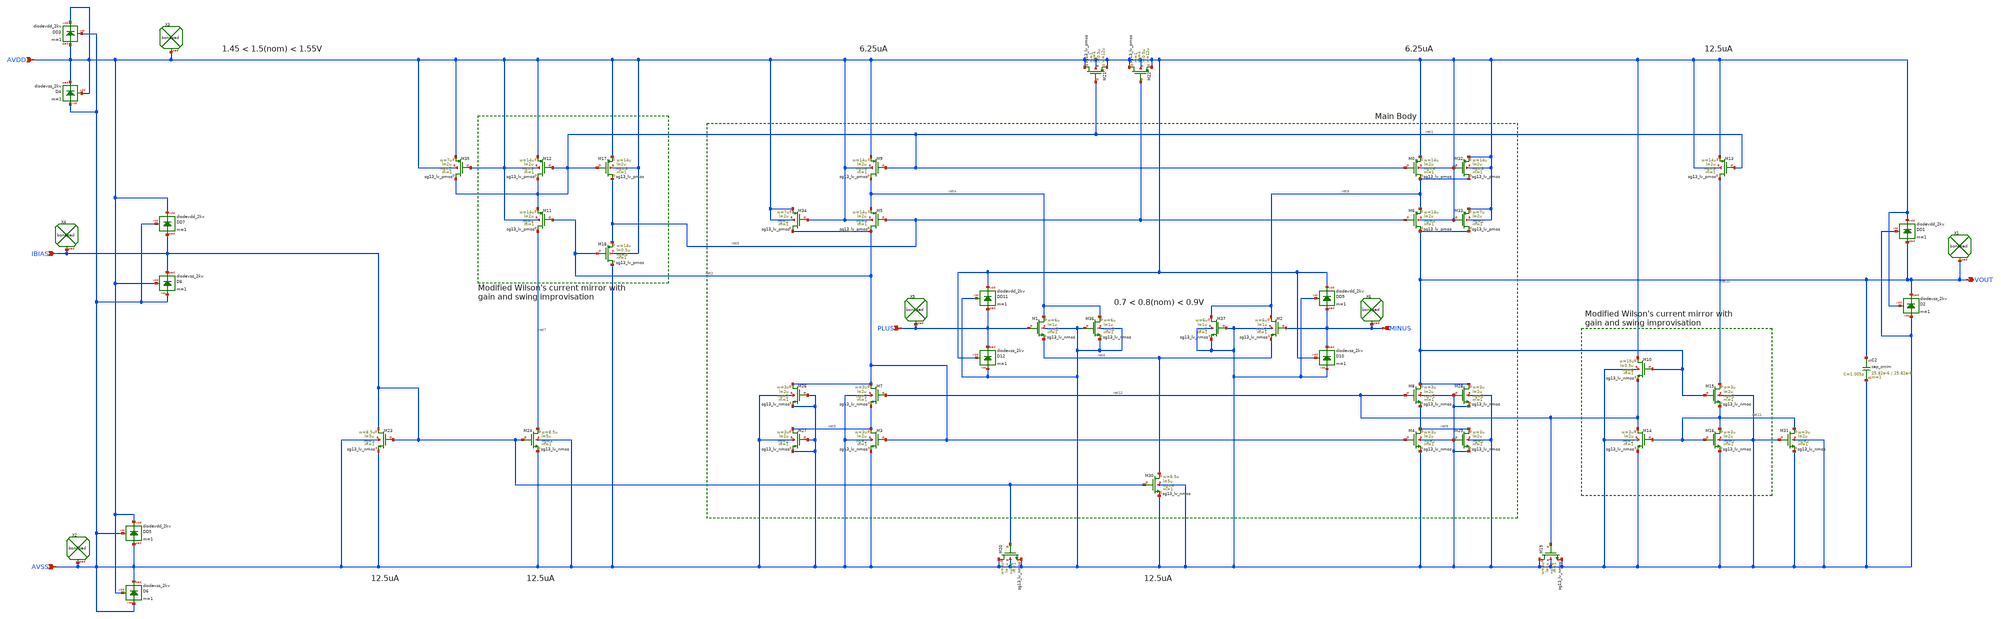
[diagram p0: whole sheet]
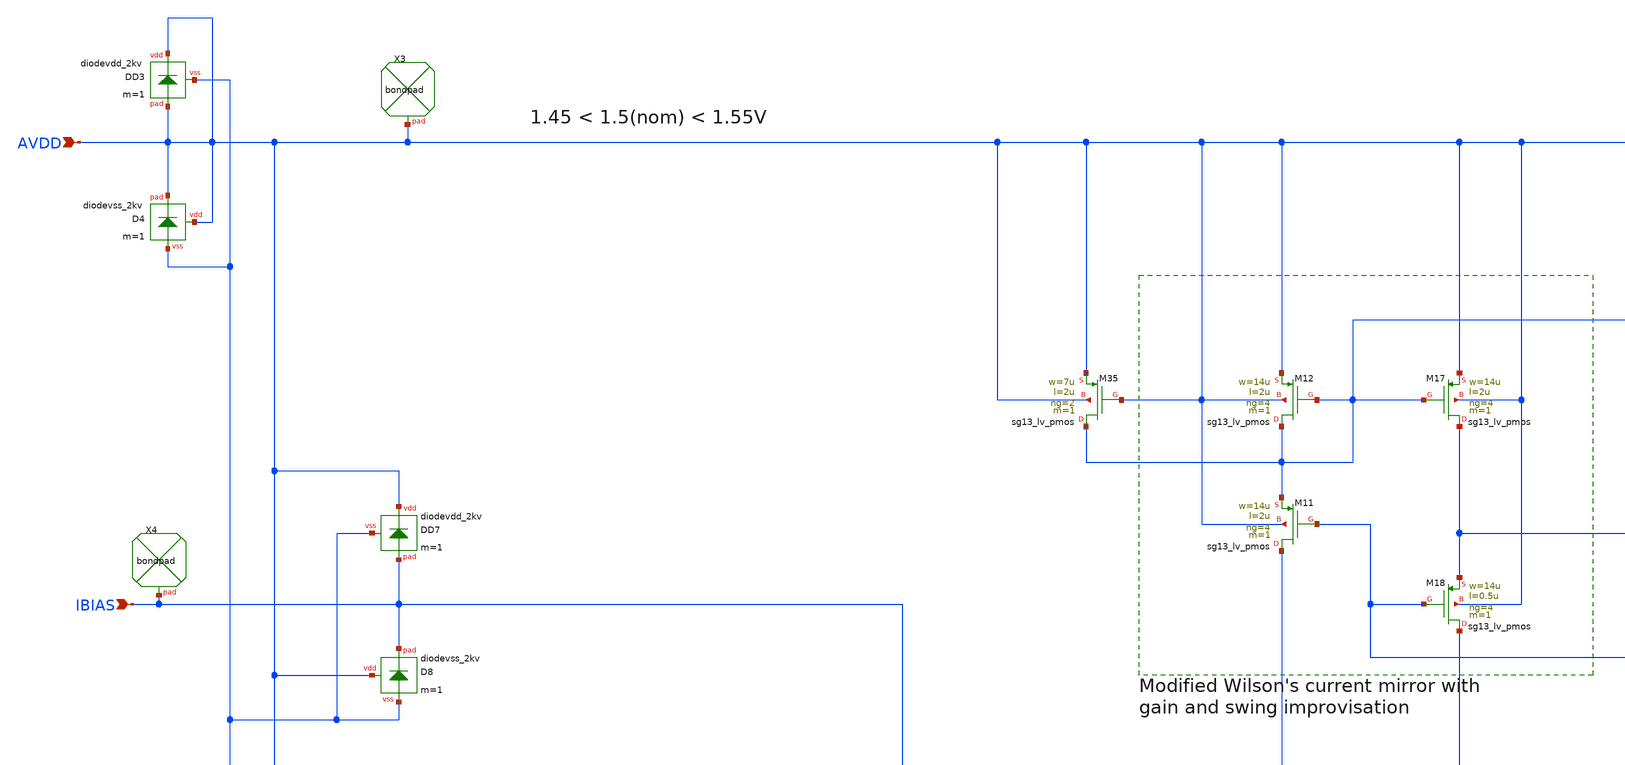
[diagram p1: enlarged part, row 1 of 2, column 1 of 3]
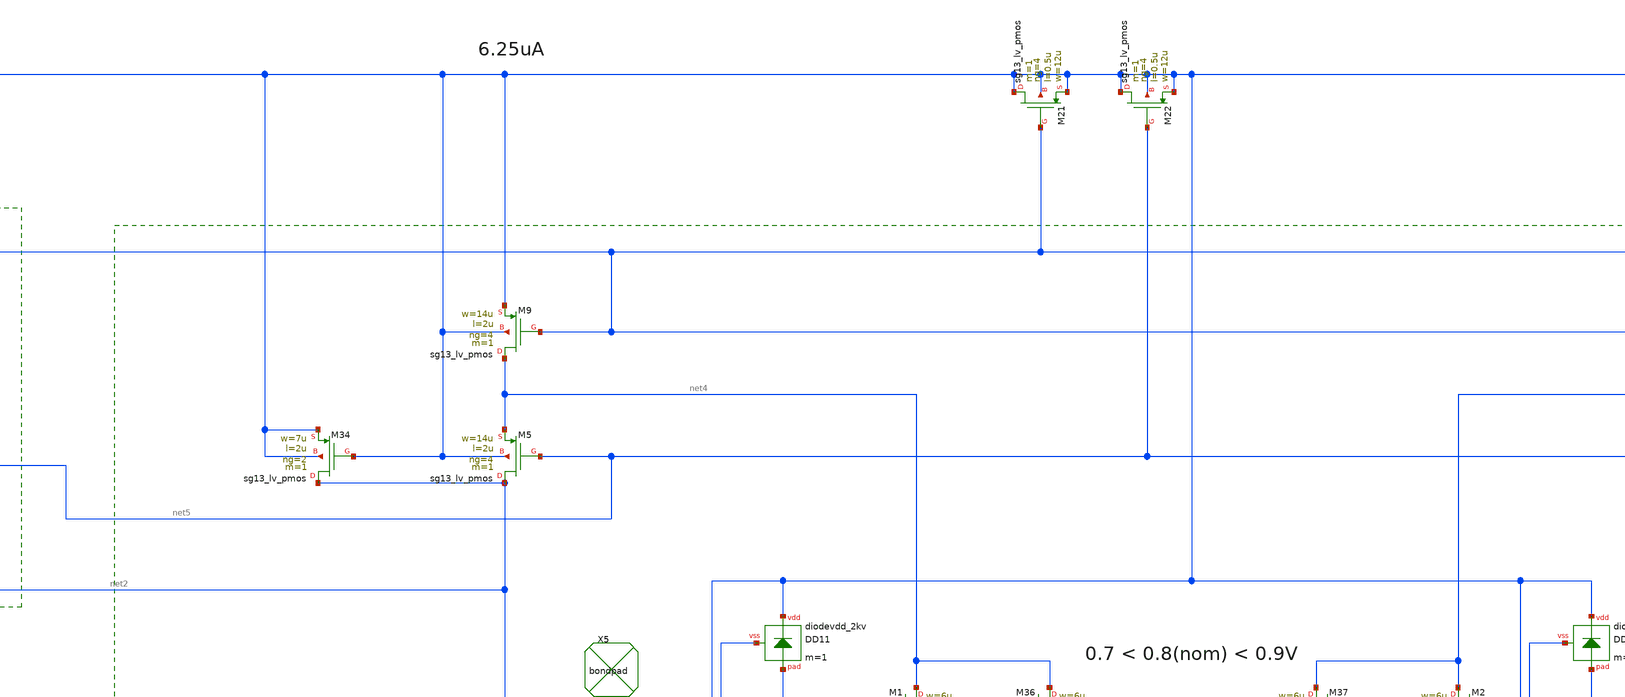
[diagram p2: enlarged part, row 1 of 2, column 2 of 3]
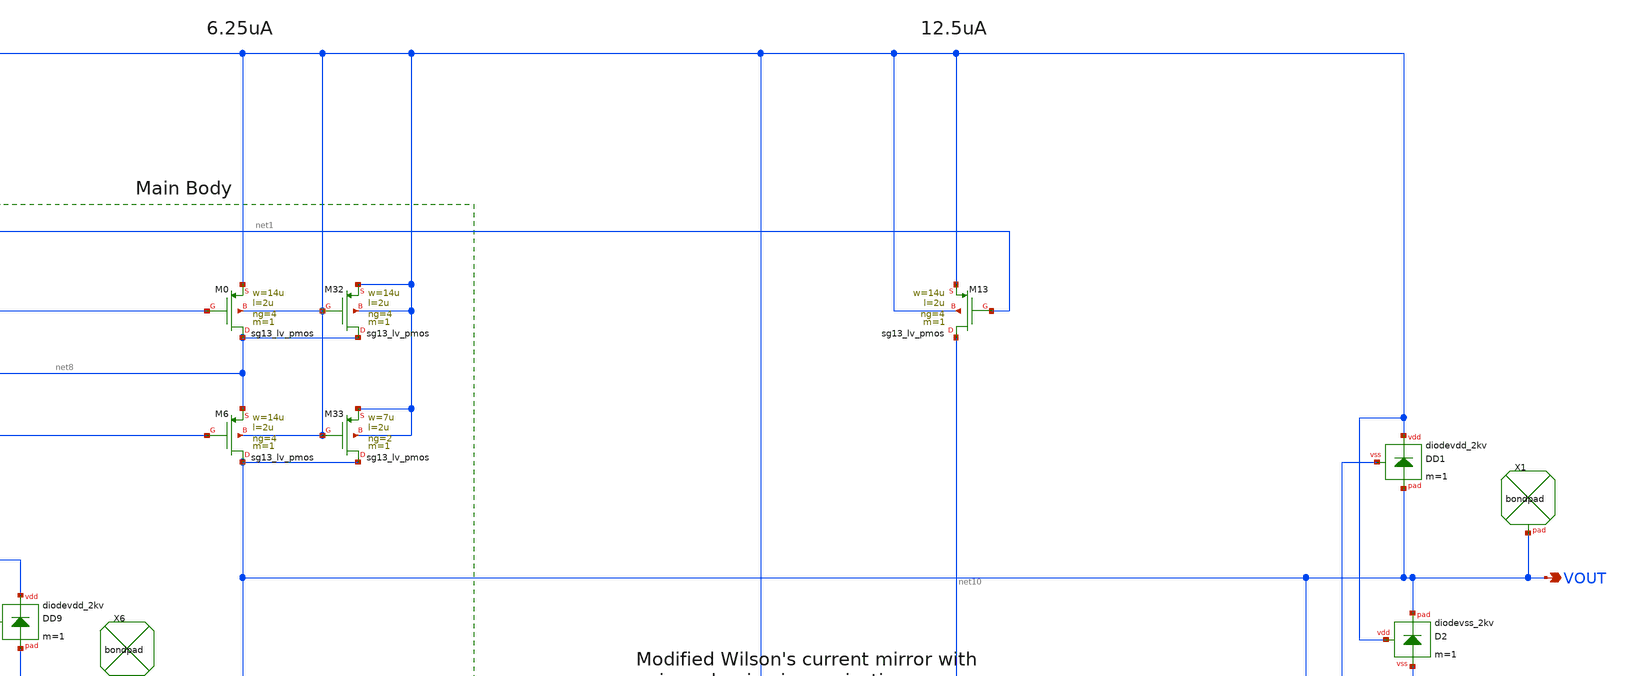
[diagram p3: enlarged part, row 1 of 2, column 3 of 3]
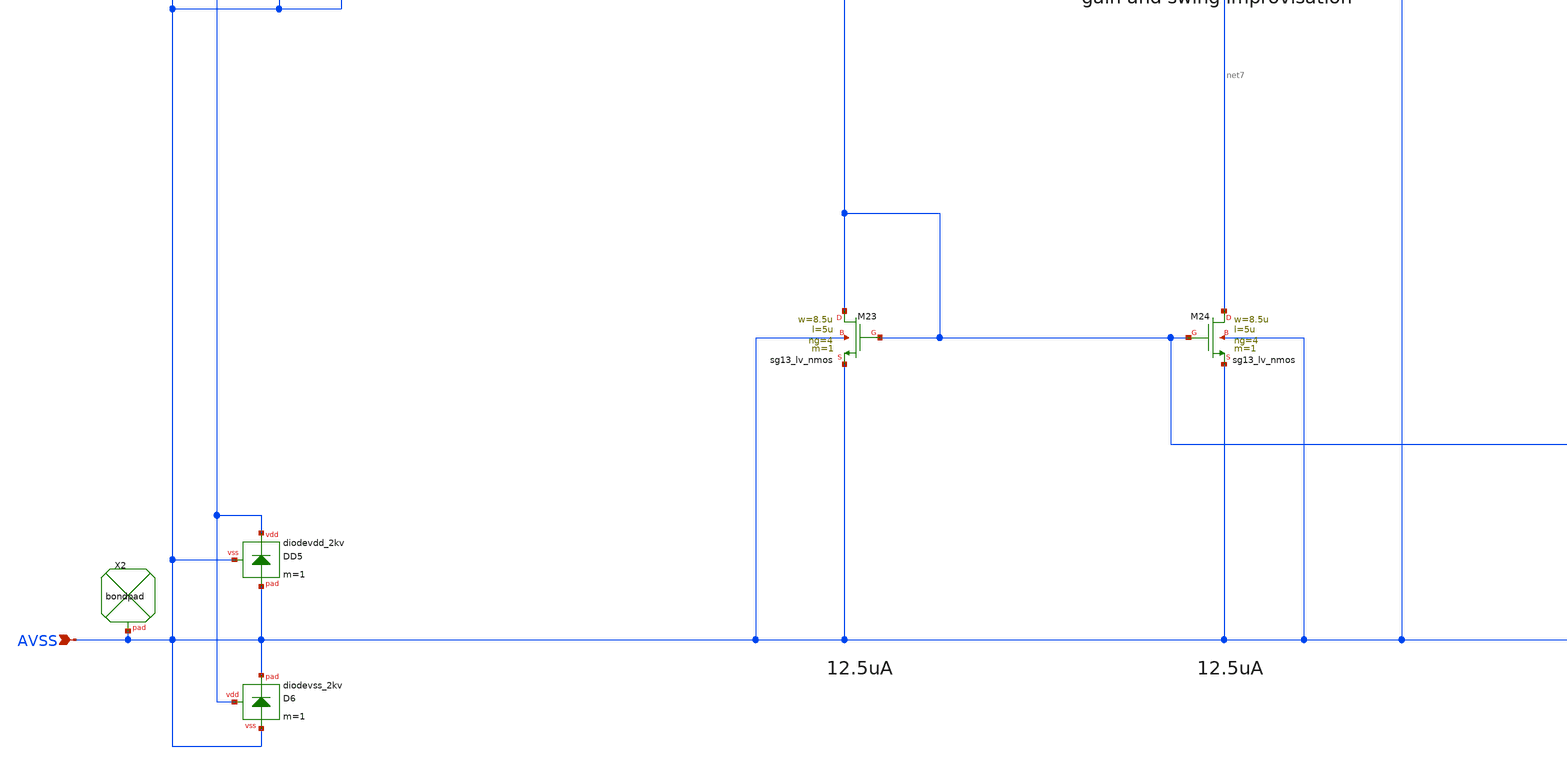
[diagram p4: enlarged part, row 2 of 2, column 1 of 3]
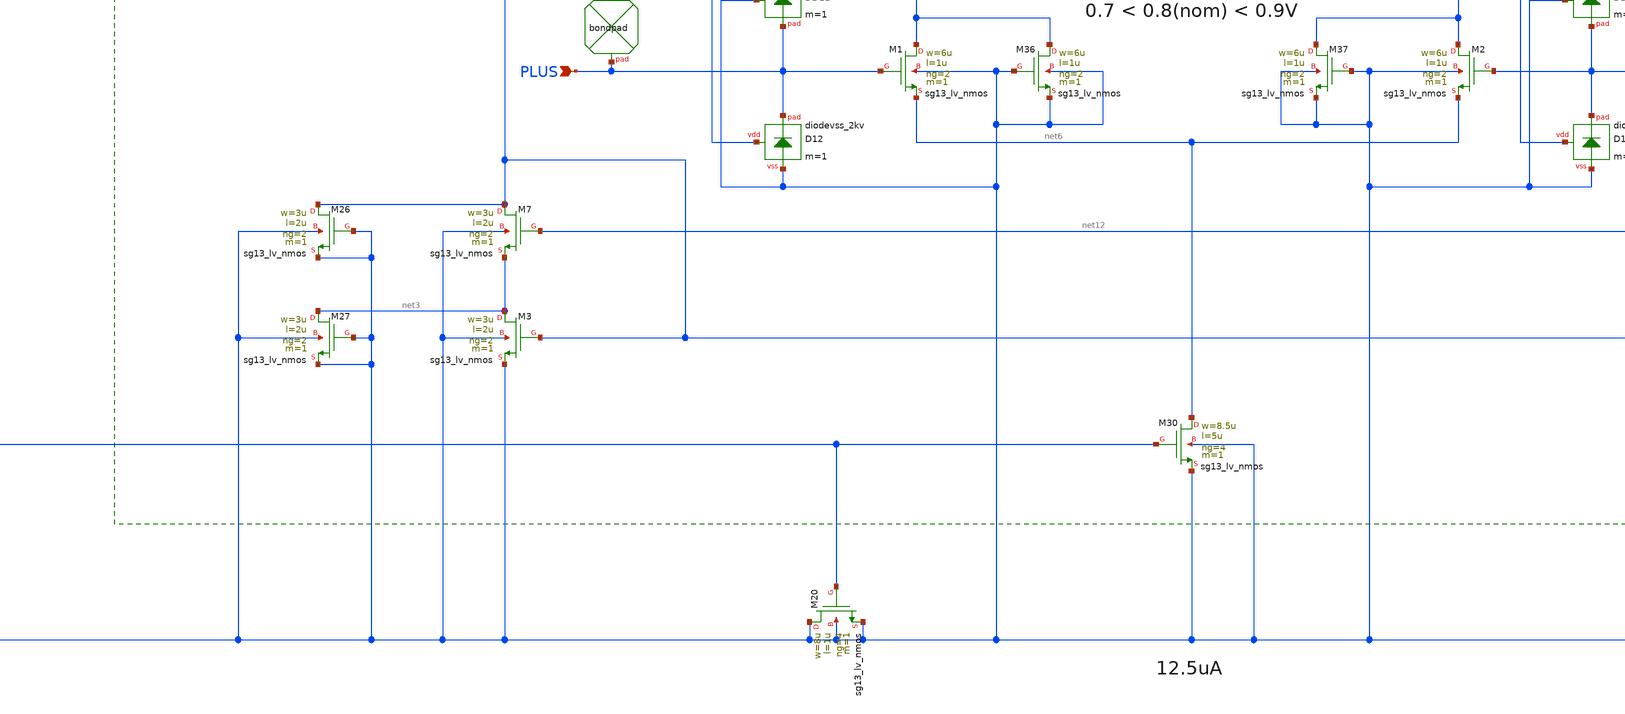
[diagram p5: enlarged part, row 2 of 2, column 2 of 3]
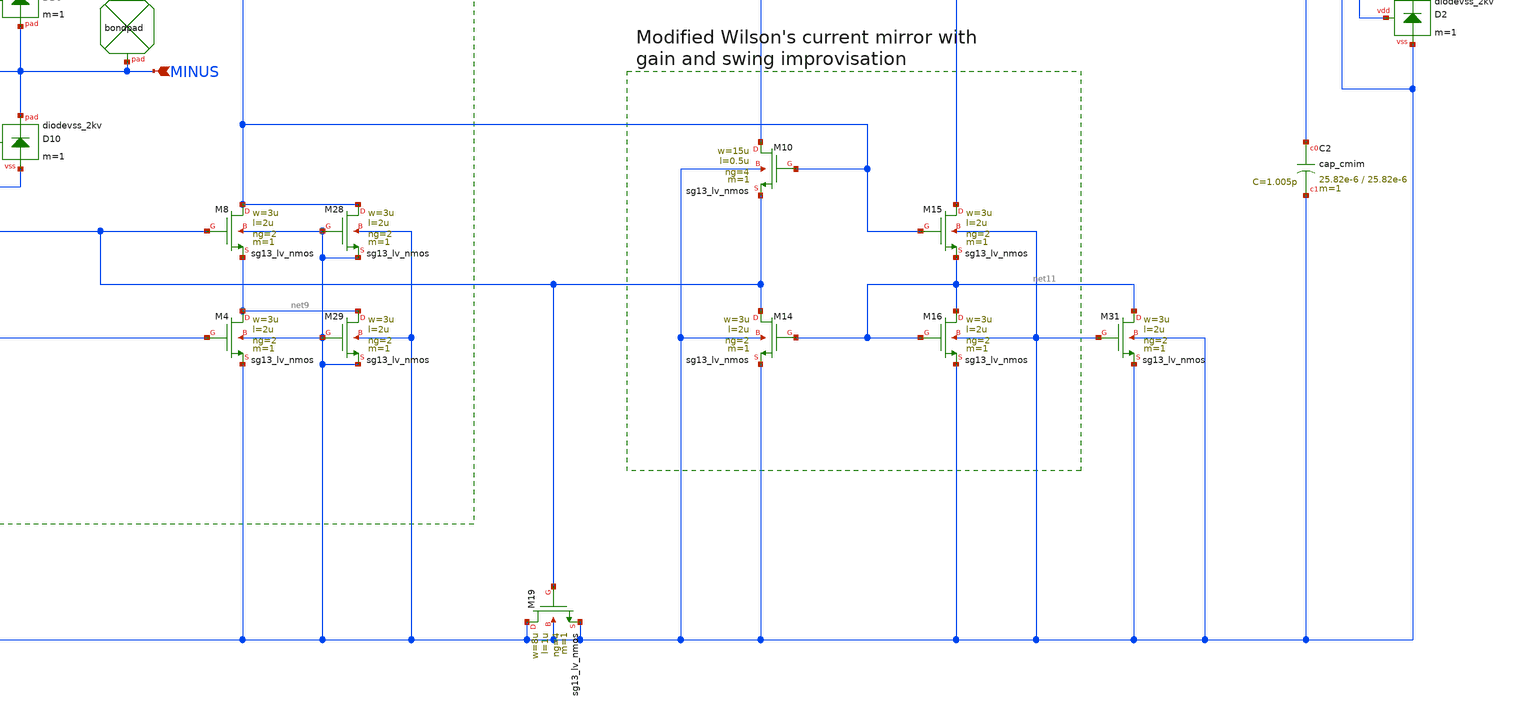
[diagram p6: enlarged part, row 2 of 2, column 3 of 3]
** sch_path: Amplifier_with_decoupling/design_data/xschem/FMD_QNC_ota_decoup.sch
* (c) 2025 Thesis_HP, Apache-2.0 license
**.subckt FMD_QNC_ota_decoup PLUS MINUS VOUT AVSS IBIAS AVDD
*.ipin PLUS
*.ipin MINUS
*.opin VOUT
*.ipin AVSS
*.ipin IBIAS
*.ipin AVDD
XM23 IBIAS IBIAS AVSS AVSS sg13_lv_nmos w=8.5u l=5u ng=4 m=1 mm_ok=1
XM24 net7 IBIAS AVSS AVSS sg13_lv_nmos w=8.5u l=5u ng=4 m=1 mm_ok=1
XM11 net7 net2 net1 AVDD sg13_lv_pmos w=14u l=2u ng=4 m=1 mm_ok=1
XM12 net1 net1 AVDD AVDD sg13_lv_pmos w=14u l=2u ng=4 m=1 mm_ok=1
XM18 AVSS net2 net5 AVDD sg13_lv_pmos w=14u l=0.5u ng=4 m=1 mm_ok=1
XM17 net5 net1 AVDD AVDD sg13_lv_pmos w=14u l=2u ng=4 m=1 mm_ok=1
XM9 net4 net1 AVDD AVDD sg13_lv_pmos w=14u l=2u ng=4 m=1 mm_ok=1
XM5 net2 net5 net4 AVDD sg13_lv_pmos w=14u l=2u ng=4 m=1 mm_ok=1
XM7 net2 net12 net3 AVSS sg13_lv_nmos w=3u l=2u ng=2 m=1 mm_ok=1
XM3 net3 net2 AVSS AVSS sg13_lv_nmos w=3u l=2u ng=2 m=1 mm_ok=1
XM30 net6 IBIAS AVSS AVSS sg13_lv_nmos w=8.5u l=5u ng=4 m=1 mm_ok=1
XM1 net4 PLUS net6 AVSS sg13_lv_nmos w=6u l=1u ng=2 m=1 mm_ok=1
XM2 net8 MINUS net6 AVSS sg13_lv_nmos w=6u l=1u ng=2 m=1 mm_ok=1
XM37 net8 AVSS AVSS AVSS sg13_lv_nmos w=6u l=1u ng=2 m=1 mm_ok=1
XM6 VOUT net5 net8 AVDD sg13_lv_pmos w=14u l=2u ng=4 m=1 mm_ok=1
XM0 net8 net1 AVDD AVDD sg13_lv_pmos w=14u l=2u ng=4 m=1 mm_ok=1
XM8 VOUT net12 net9 AVSS sg13_lv_nmos w=3u l=2u ng=2 m=1 mm_ok=1
XM4 net9 net2 AVSS AVSS sg13_lv_nmos w=3u l=2u ng=2 m=1 mm_ok=1
XM29 net9 AVSS AVSS AVSS sg13_lv_nmos w=3u l=2u ng=2 m=1 mm_ok=1
XM28 VOUT AVSS AVSS AVSS sg13_lv_nmos w=3u l=2u ng=2 m=1 mm_ok=1
XM32 net8 AVDD AVDD AVDD sg13_lv_pmos w=14u l=2u ng=4 m=1 mm_ok=1
XM33 VOUT AVDD AVDD AVDD sg13_lv_pmos w=7u l=2u ng=2 m=1 mm_ok=1
XM13 net10 net1 AVDD AVDD sg13_lv_pmos w=14u l=2u ng=4 m=1 mm_ok=1
XM15 net10 VOUT net11 AVSS sg13_lv_nmos w=3u l=2u ng=2 m=1 mm_ok=1
XM16 net11 net11 AVSS AVSS sg13_lv_nmos w=3u l=2u ng=2 m=1 mm_ok=1
XM14 net12 net11 AVSS AVSS sg13_lv_nmos w=3u l=2u ng=2 m=1 mm_ok=1
XM10 AVDD VOUT net12 AVSS sg13_lv_nmos w=15u l=0.5u ng=4 m=1 mm_ok=1
XM36 net4 AVSS AVSS AVSS sg13_lv_nmos w=6u l=1u ng=2 m=1 mm_ok=1
XM34 net2 AVDD AVDD AVDD sg13_lv_pmos w=7u l=2u ng=2 m=1 mm_ok=1
XM27 net3 AVSS AVSS AVSS sg13_lv_nmos w=3u l=2u ng=2 m=1 mm_ok=1
XM26 net2 AVSS AVSS AVSS sg13_lv_nmos w=3u l=2u ng=2 m=1 mm_ok=1
XM35 net1 AVDD AVDD AVDD sg13_lv_pmos w=7u l=2u ng=2 m=1 mm_ok=1
XM31 net11 AVSS AVSS AVSS sg13_lv_nmos w=3u l=2u ng=2 m=1 mm_ok=1
XC2 VOUT AVSS cap_cmim w=25.82e-6 l=25.82e-6 m=1 mm_ok=1
XM19 AVSS net12 AVSS AVSS sg13_lv_nmos w=8u l=1u ng=4 m=1 mm_ok=1
XM20 AVSS IBIAS AVSS AVSS sg13_lv_nmos w=8u l=1u ng=4 m=1 mm_ok=1
XM21 AVDD net1 AVDD AVDD sg13_lv_pmos w=12u l=0.5u ng=4 m=1 mm_ok=1
XM22 AVDD net5 AVDD AVDD sg13_lv_pmos w=12u l=0.5u ng=4 m=1 mm_ok=1
XX1 VOUT bondpad size=80u shape=0 padtype=0
XD1 AVDD VOUT AVSS diodevdd_2kv m=1
XD2 AVDD VOUT AVSS diodevss_2kv m=1
XX5 PLUS bondpad size=80u shape=0 padtype=0
XD9 AVDD MINUS AVSS diodevdd_2kv m=1
XD10 AVDD MINUS AVSS diodevss_2kv m=1
XX6 MINUS bondpad size=80u shape=0 padtype=0
XD11 AVDD PLUS AVSS diodevdd_2kv m=1
XD12 AVDD PLUS AVSS diodevss_2kv m=1
XD3 AVDD AVDD AVSS diodevdd_2kv m=1
XD4 AVDD AVDD AVSS diodevss_2kv m=1
XD5 AVDD AVSS AVSS diodevdd_2kv m=1
XD6 AVDD AVSS AVSS diodevss_2kv m=1
XX2 AVSS bondpad size=80u shape=0 padtype=0
XX3 AVDD bondpad size=80u shape=0 padtype=0
XD7 AVDD IBIAS AVSS diodevdd_2kv m=1
XD8 AVDD IBIAS AVSS diodevss_2kv m=1
XX4 IBIAS bondpad size=80u shape=0 padtype=0
**.ends
.end
